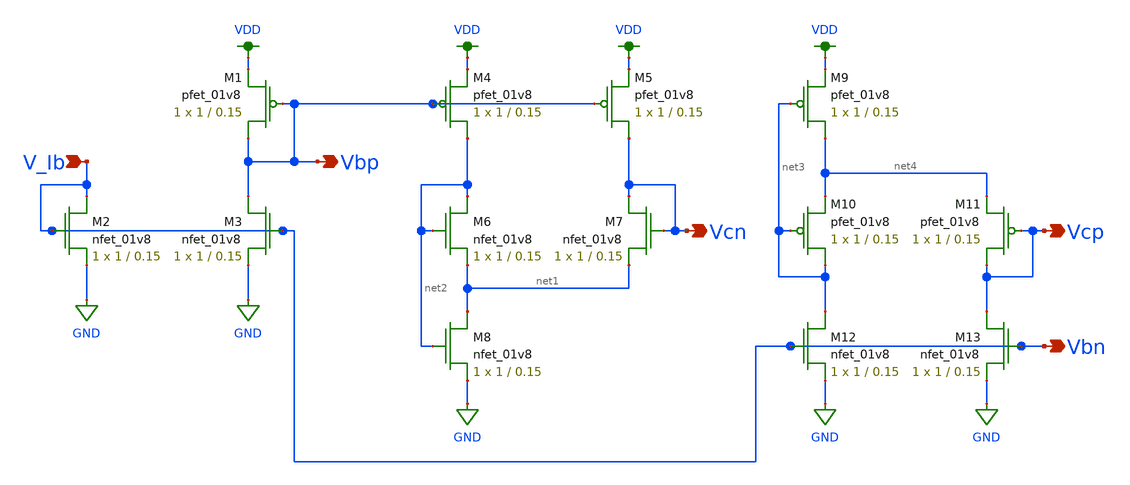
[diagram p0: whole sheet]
** sch_path: MP3/xschem/cascode_v_gen.sch
**.subckt cascode_v_gen Vcn Vbn Vcp Vbp V_Ib
*.opin Vcn
*.opin Vbn
*.opin Vcp
*.opin Vbp
*.ipin V_Ib
XM4 net2 Vbp VDD VDD sky130_fd_pr__pfet_01v8 L=0.15 W=1 nf=1 ad='int((nf+1)/2) * W/nf * 0.29' as='int((nf+2)/2) * W/nf * 0.29'
+ pd='2*int((nf+1)/2) * (W/nf + 0.29)' ps='2*int((nf+2)/2) * (W/nf + 0.29)' nrd='0.29 / W' nrs='0.29 / W'
+ sa=0 sb=0 sd=0 mult=1 m=1
XM5 Vcn Vbp VDD VDD sky130_fd_pr__pfet_01v8 L=0.15 W=1 nf=1 ad='int((nf+1)/2) * W/nf * 0.29' as='int((nf+2)/2) * W/nf * 0.29'
+ pd='2*int((nf+1)/2) * (W/nf + 0.29)' ps='2*int((nf+2)/2) * (W/nf + 0.29)' nrd='0.29 / W' nrs='0.29 / W'
+ sa=0 sb=0 sd=0 mult=1 m=1
XM6 net2 net2 net1 GND sky130_fd_pr__nfet_01v8 L=0.15 W=1 nf=1 ad='int((nf+1)/2) * W/nf * 0.29' as='int((nf+2)/2) * W/nf * 0.29'
+ pd='2*int((nf+1)/2) * (W/nf + 0.29)' ps='2*int((nf+2)/2) * (W/nf + 0.29)' nrd='0.29 / W' nrs='0.29 / W'
+ sa=0 sb=0 sd=0 mult=1 m=1
XM7 Vcn Vcn net1 GND sky130_fd_pr__nfet_01v8 L=0.15 W=1 nf=1 ad='int((nf+1)/2) * W/nf * 0.29' as='int((nf+2)/2) * W/nf * 0.29'
+ pd='2*int((nf+1)/2) * (W/nf + 0.29)' ps='2*int((nf+2)/2) * (W/nf + 0.29)' nrd='0.29 / W' nrs='0.29 / W'
+ sa=0 sb=0 sd=0 mult=1 m=1
XM8 net1 net2 GND GND sky130_fd_pr__nfet_01v8 L=0.15 W=1 nf=1 ad='int((nf+1)/2) * W/nf * 0.29' as='int((nf+2)/2) * W/nf * 0.29'
+ pd='2*int((nf+1)/2) * (W/nf + 0.29)' ps='2*int((nf+2)/2) * (W/nf + 0.29)' nrd='0.29 / W' nrs='0.29 / W'
+ sa=0 sb=0 sd=0 mult=1 m=1
XM1 Vbp Vbp VDD VDD sky130_fd_pr__pfet_01v8 L=0.15 W=1 nf=1 ad='int((nf+1)/2) * W/nf * 0.29' as='int((nf+2)/2) * W/nf * 0.29'
+ pd='2*int((nf+1)/2) * (W/nf + 0.29)' ps='2*int((nf+2)/2) * (W/nf + 0.29)' nrd='0.29 / W' nrs='0.29 / W'
+ sa=0 sb=0 sd=0 mult=1 m=1
XM2 Vbn Vbn GND GND sky130_fd_pr__nfet_01v8 L=0.15 W=1 nf=1 ad='int((nf+1)/2) * W/nf * 0.29' as='int((nf+2)/2) * W/nf * 0.29'
+ pd='2*int((nf+1)/2) * (W/nf + 0.29)' ps='2*int((nf+2)/2) * (W/nf + 0.29)' nrd='0.29 / W' nrs='0.29 / W'
+ sa=0 sb=0 sd=0 mult=1 m=1
XM3 Vbp Vbn GND GND sky130_fd_pr__nfet_01v8 L=0.15 W=1 nf=1 ad='int((nf+1)/2) * W/nf * 0.29' as='int((nf+2)/2) * W/nf * 0.29'
+ pd='2*int((nf+1)/2) * (W/nf + 0.29)' ps='2*int((nf+2)/2) * (W/nf + 0.29)' nrd='0.29 / W' nrs='0.29 / W'
+ sa=0 sb=0 sd=0 mult=1 m=1
XM9 net4 net3 VDD VDD sky130_fd_pr__pfet_01v8 L=0.15 W=1 nf=1 ad='int((nf+1)/2) * W/nf * 0.29' as='int((nf+2)/2) * W/nf * 0.29'
+ pd='2*int((nf+1)/2) * (W/nf + 0.29)' ps='2*int((nf+2)/2) * (W/nf + 0.29)' nrd='0.29 / W' nrs='0.29 / W'
+ sa=0 sb=0 sd=0 mult=1 m=1
XM10 net3 net3 net4 VDD sky130_fd_pr__pfet_01v8 L=0.15 W=1 nf=1 ad='int((nf+1)/2) * W/nf * 0.29' as='int((nf+2)/2) * W/nf * 0.29'
+ pd='2*int((nf+1)/2) * (W/nf + 0.29)' ps='2*int((nf+2)/2) * (W/nf + 0.29)' nrd='0.29 / W' nrs='0.29 / W'
+ sa=0 sb=0 sd=0 mult=1 m=1
XM11 Vcp Vcp net4 VDD sky130_fd_pr__pfet_01v8 L=0.15 W=1 nf=1 ad='int((nf+1)/2) * W/nf * 0.29' as='int((nf+2)/2) * W/nf * 0.29'
+ pd='2*int((nf+1)/2) * (W/nf + 0.29)' ps='2*int((nf+2)/2) * (W/nf + 0.29)' nrd='0.29 / W' nrs='0.29 / W'
+ sa=0 sb=0 sd=0 mult=1 m=1
XM12 net3 Vbn GND GND sky130_fd_pr__nfet_01v8 L=0.15 W=1 nf=1 ad='int((nf+1)/2) * W/nf * 0.29' as='int((nf+2)/2) * W/nf * 0.29'
+ pd='2*int((nf+1)/2) * (W/nf + 0.29)' ps='2*int((nf+2)/2) * (W/nf + 0.29)' nrd='0.29 / W' nrs='0.29 / W'
+ sa=0 sb=0 sd=0 mult=1 m=1
XM13 Vcp Vbn GND GND sky130_fd_pr__nfet_01v8 L=0.15 W=1 nf=1 ad='int((nf+1)/2) * W/nf * 0.29' as='int((nf+2)/2) * W/nf * 0.29'
+ pd='2*int((nf+1)/2) * (W/nf + 0.29)' ps='2*int((nf+2)/2) * (W/nf + 0.29)' nrd='0.29 / W' nrs='0.29 / W'
+ sa=0 sb=0 sd=0 mult=1 m=1
**.ends
.GLOBAL VDD
.GLOBAL GND
.end
